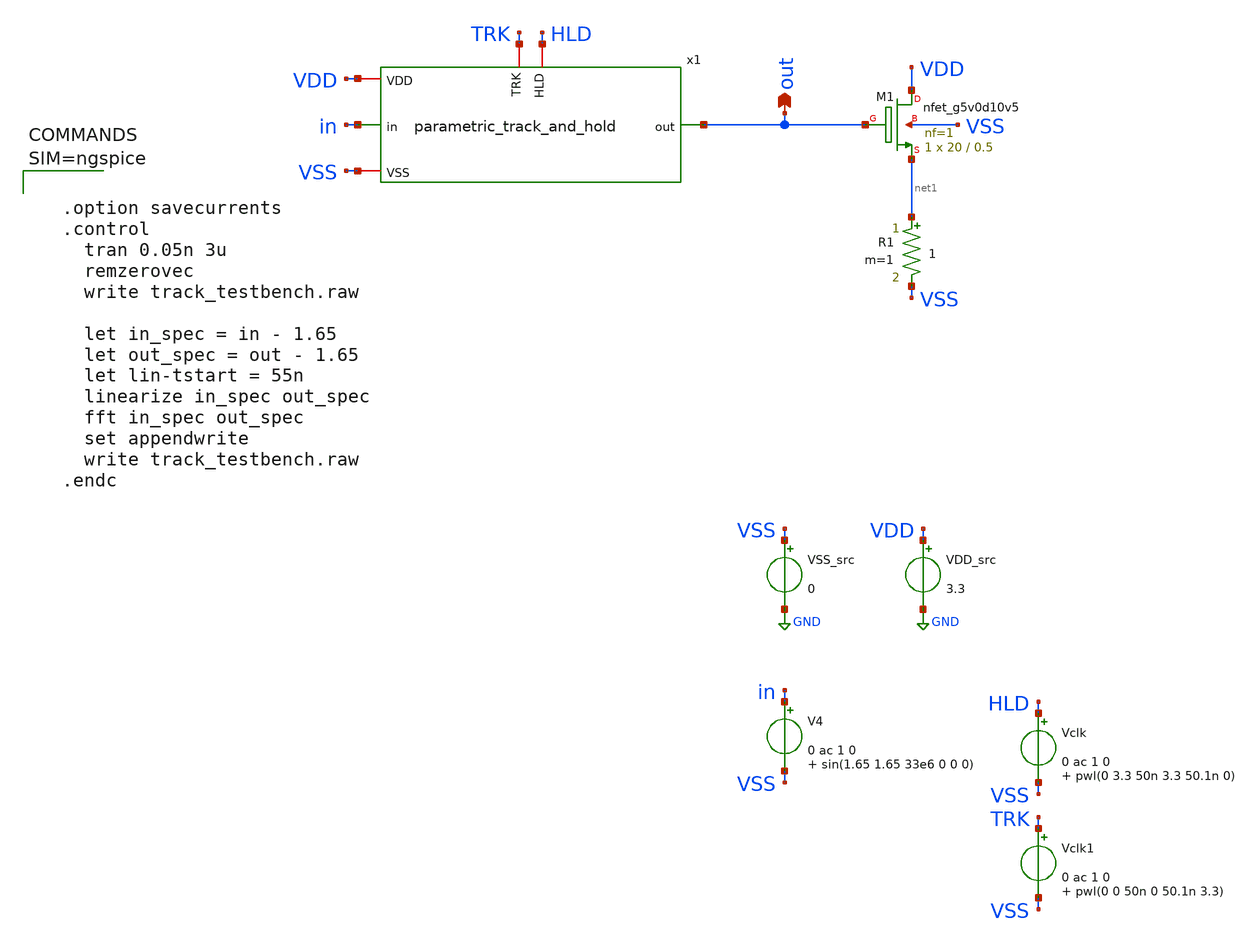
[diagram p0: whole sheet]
** sch_path: xschem/track_testbench.sch
**.subckt track_testbench out
*.opin out
VDD_src VDD GND 3.3
VSS_src VSS GND 0
V4 in VSS 0 ac 1 0 sin(1.65 1.65 33e6 0 0 0)
XM1 VDD out net1 VSS sky130_fd_pr__nfet_g5v0d10v5 L=0.5 W=20 nf=1 ad='int((nf+1)/2) * W/nf * 0.29' as='int((nf+2)/2) * W/nf * 0.29'
+ pd='2*int((nf+1)/2) * (W/nf + 0.29)' ps='2*int((nf+2)/2) * (W/nf + 0.29)' nrd='0.29 / W' nrs='0.29 / W'
+ sa=0 sb=0 sd=0 mult=1 m=1
R1 net1 VSS 1 m=1
Vclk HLD VSS 0 ac 1 0 pwl(0 3.3 50n 3.3 50.1n 0)
Vclk1 TRK VSS 0 ac 1 0 pwl(0 0 50n 0 50.1n 3.3)
x1 HLD TRK VDD VSS out in parametric_track_and_hold WT=1 PFT=1.21 PF=2 WS=5 WB=5 CB=18
**** begin user architecture code

** opencircuitdesign pdks install
.lib $::SKYWATER_MODELS/sky130.lib.spice tt





  .option savecurrents
  .control
    tran 0.05n 3u
    remzerovec
    write track_testbench.raw

    let in_spec = in - 1.65
    let out_spec = out - 1.65
    let lin-tstart = 55n
    linearize in_spec out_spec
    fft in_spec out_spec
    set appendwrite
    write track_testbench.raw
  .endc



**** end user architecture code
**.ends

* expanding   symbol:  parametric_track_and_hold.sym # of pins=6
** sym_path: xschem/parametric_track_and_hold.sym
** sch_path: xschem/parametric_track_and_hold.sch
.subckt parametric_track_and_hold HLD TRK VDD VSS out in  WT=1 PFT=1.21 PF=2 WS=5 WB=5 CB=18
*.iopin VSS
*.iopin VDD
*.ipin in
*.opin out
*.iopin TRK
*.iopin HLD
XC1 out VSS sky130_fd_pr__cap_mim_m3_1 W=5 L=5 MF=1 m=1
XM1 out X in VSS sky130_fd_pr__nfet_g5v0d10v5 L=0.5 W={WT} nf=1 ad='int((nf+1)/2) * W/nf * 0.29' as='int((nf+2)/2) * W/nf * 0.29'
+ pd='2*int((nf+1)/2) * (W/nf + 0.29)' ps='2*int((nf+2)/2) * (W/nf + 0.29)' nrd='0.29 / W' nrs='0.29 / W'
+ sa=0 sb=0 sd=0 mult=1 m=1
XM1p out net1 in VDD sky130_fd_pr__pfet_g5v0d10v5 L=0.5 W={WT*PFT} nf=1 ad='int((nf+1)/2) * W/nf * 0.29'
+ as='int((nf+2)/2) * W/nf * 0.29' pd='2*int((nf+1)/2) * (W/nf + 0.29)' ps='2*int((nf+2)/2) * (W/nf + 0.29)'
+ nrd='0.29 / W' nrs='0.29 / W' sa=0 sb=0 sd=0 mult=1 m=1
XM4 VSS HLD X VSS sky130_fd_pr__nfet_g5v0d10v5 L=0.5 W={WS} nf=1 ad='int((nf+1)/2) * W/nf * 0.29' as='int((nf+2)/2) * W/nf * 0.29'
+ pd='2*int((nf+1)/2) * (W/nf + 0.29)' ps='2*int((nf+2)/2) * (W/nf + 0.29)' nrd='0.29 / W' nrs='0.29 / W'
+ sa=0 sb=0 sd=0 mult=1 m=1
XM4p net1 TRK VDD VDD sky130_fd_pr__pfet_g5v0d10v5 L=0.5 W={WS*PF} nf=1 ad='int((nf+1)/2) * W/nf * 0.29'
+ as='int((nf+2)/2) * W/nf * 0.29' pd='2*int((nf+1)/2) * (W/nf + 0.29)' ps='2*int((nf+2)/2) * (W/nf + 0.29)'
+ nrd='0.29 / W' nrs='0.29 / W' sa=0 sb=0 sd=0 mult=1 m=1
XM2 X HLD P P sky130_fd_pr__pfet_g5v0d10v5 L=0.5 W={WS*PF} nf=1 ad='int((nf+1)/2) * W/nf * 0.29' as='int((nf+2)/2) * W/nf * 0.29'
+ pd='2*int((nf+1)/2) * (W/nf + 0.29)' ps='2*int((nf+2)/2) * (W/nf + 0.29)' nrd='0.29 / W' nrs='0.29 / W'
+ sa=0 sb=0 sd=0 mult=1 m=1
XM2p net2 TRK net1 net2 sky130_fd_pr__nfet_g5v0d10v5 L=0.5 W={WS} nf=1 ad='int((nf+1)/2) * W/nf * 0.29'
+ as='int((nf+2)/2) * W/nf * 0.29' pd='2*int((nf+1)/2) * (W/nf + 0.29)' ps='2*int((nf+2)/2) * (W/nf + 0.29)'
+ nrd='0.29 / W' nrs='0.29 / W' sa=0 sb=0 sd=0 mult=1 m=1
XM3 in X Q VSS sky130_fd_pr__nfet_g5v0d10v5 L=0.5 W={WB} nf=1 ad='int((nf+1)/2) * W/nf * 0.29' as='int((nf+2)/2) * W/nf * 0.29'
+ pd='2*int((nf+1)/2) * (W/nf + 0.29)' ps='2*int((nf+2)/2) * (W/nf + 0.29)' nrd='0.29 / W' nrs='0.29 / W'
+ sa=0 sb=0 sd=0 mult=1 m=1
XM6 Q HLD VSS VSS sky130_fd_pr__nfet_g5v0d10v5 L=0.5 W={WB} nf=1 ad='int((nf+1)/2) * W/nf * 0.29' as='int((nf+2)/2) * W/nf * 0.29'
+ pd='2*int((nf+1)/2) * (W/nf + 0.29)' ps='2*int((nf+2)/2) * (W/nf + 0.29)' nrd='0.29 / W' nrs='0.29 / W'
+ sa=0 sb=0 sd=0 mult=1 m=1
XM3p net3 net1 in VDD sky130_fd_pr__pfet_g5v0d10v5 L=0.5 W={WB*PF} nf=1 ad='int((nf+1)/2) * W/nf * 0.29'
+ as='int((nf+2)/2) * W/nf * 0.29' pd='2*int((nf+1)/2) * (W/nf + 0.29)' ps='2*int((nf+2)/2) * (W/nf + 0.29)'
+ nrd='0.29 / W' nrs='0.29 / W' sa=0 sb=0 sd=0 mult=1 m=1
XM6p VDD TRK net3 VDD sky130_fd_pr__pfet_g5v0d10v5 L=0.5 W={WB*PF} nf=1 ad='int((nf+1)/2) * W/nf * 0.29'
+ as='int((nf+2)/2) * W/nf * 0.29' pd='2*int((nf+1)/2) * (W/nf + 0.29)' ps='2*int((nf+2)/2) * (W/nf + 0.29)'
+ nrd='0.29 / W' nrs='0.29 / W' sa=0 sb=0 sd=0 mult=1 m=1
XM5 P X VDD P sky130_fd_pr__pfet_g5v0d10v5 L=0.5 W={WB*PF} nf=1 ad='int((nf+1)/2) * W/nf * 0.29' as='int((nf+2)/2) * W/nf * 0.29'
+ pd='2*int((nf+1)/2) * (W/nf + 0.29)' ps='2*int((nf+2)/2) * (W/nf + 0.29)' nrd='0.29 / W' nrs='0.29 / W'
+ sa=0 sb=0 sd=0 mult=1 m=1
XCb P Q sky130_fd_pr__cap_mim_m3_1 W={CB} L={CB} MF=1 m=1
XCbp net2 net3 sky130_fd_pr__cap_mim_m3_1 W={CB} L={CB} MF=1 m=1
XM5p VSS net1 net2 net2 sky130_fd_pr__nfet_g5v0d10v5 L=0.5 W={WB*PF} nf=1 ad='int((nf+1)/2) * W/nf * 0.29'
+ as='int((nf+2)/2) * W/nf * 0.29' pd='2*int((nf+1)/2) * (W/nf + 0.29)' ps='2*int((nf+2)/2) * (W/nf + 0.29)'
+ nrd='0.29 / W' nrs='0.29 / W' sa=0 sb=0 sd=0 mult=1 m=1
.ends

.GLOBAL GND
.end
